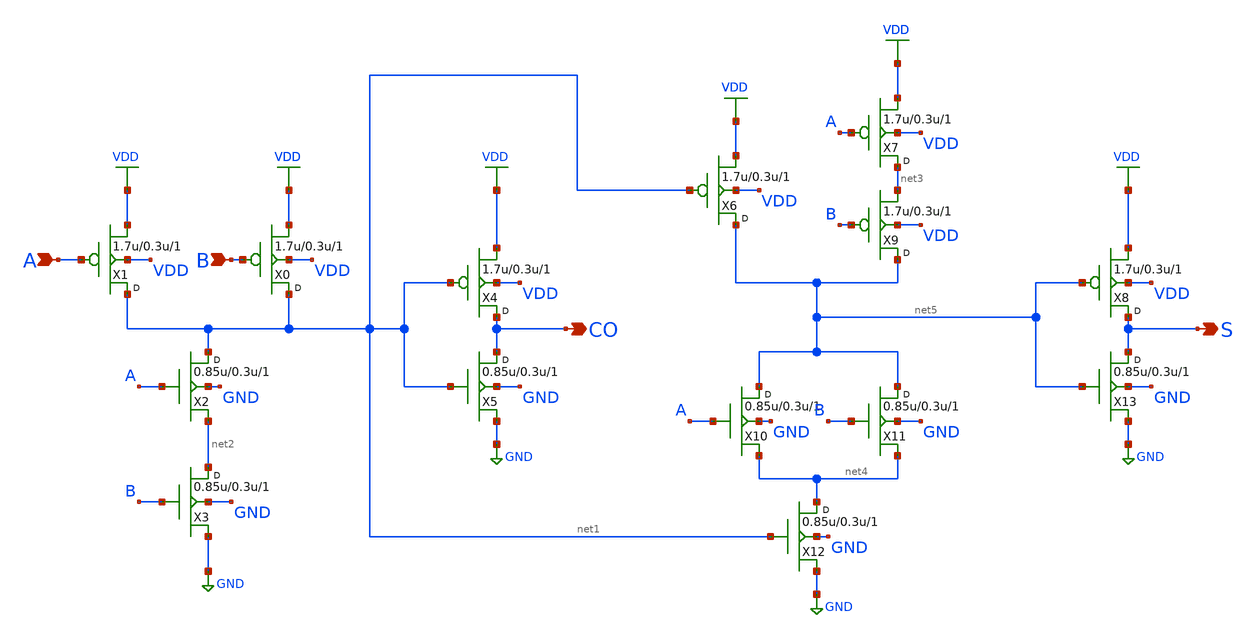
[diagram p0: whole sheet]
** sch_path: openfasoc/common/platforms/gf180mcuosu9Taddh1/gf180mcu_osu_sc_addh_1.sch
**.subckt gf180mcu_osu_sc_addh_1 A B CO S
*.ipin A
*.ipin B
*.opin CO
*.opin S
X1 net1 A VDD VDD pmos_3p3 w=1.7u l=0.3u m=1
X0 net1 B VDD VDD pmos_3p3 w=1.7u l=0.3u m=1
X2 net1 A net2 GND nmos_3p3 w=0.85u l=0.3u m=1
X3 net2 B GND GND nmos_3p3 w=0.85u l=0.3u m=1
X4 CO net1 VDD VDD pmos_3p3 w=1.7u l=0.3u m=1
X5 CO net1 GND GND nmos_3p3 w=0.85u l=0.3u m=1
X6 net5 net1 VDD VDD pmos_3p3 w=1.7u l=0.3u m=1
X7 net3 A VDD VDD pmos_3p3 w=1.7u l=0.3u m=1
X9 net5 B net3 VDD pmos_3p3 w=1.7u l=0.3u m=1
X10 net5 A net4 GND nmos_3p3 w=0.85u l=0.3u m=1
X11 net5 B net4 GND nmos_3p3 w=0.85u l=0.3u m=1
X12 net4 net1 GND GND nmos_3p3 w=0.85u l=0.3u m=1
X8 S net5 VDD VDD pmos_3p3 w=1.7u l=0.3u m=1
X13 S net5 GND GND nmos_3p3 w=0.85u l=0.3u m=1
**.ends
.GLOBAL VDD
.GLOBAL GND
.end
